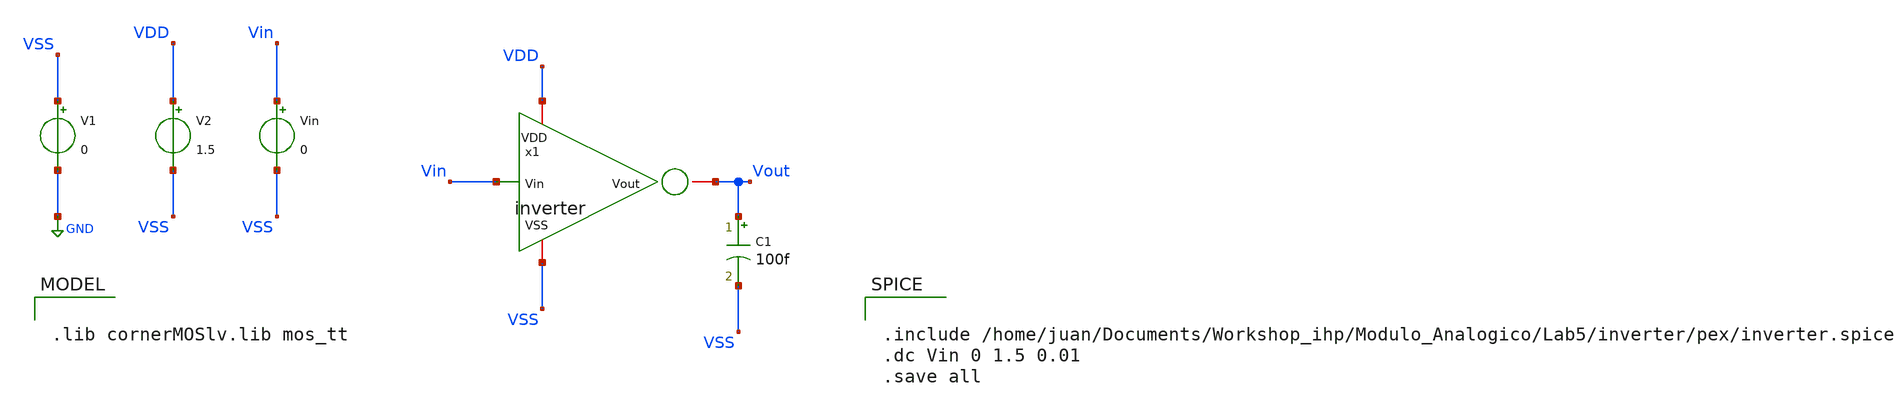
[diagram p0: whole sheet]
** sch_path: Modulo_Analogico/Lab5/inverter/pex/inverter_tb.sch
**.subckt inverter_tb
C1 Vout VSS 100f m=1
V1 VSS GND 0
V2 VDD VSS 1.5
Vin Vin VSS 0
x1 Vin VDD VSS Vout inverter
**** begin user architecture code


.include /home/juan/Documents/Workshop_ihp/Modulo_Analogico/Lab5/inverter/pex/inverter.spice
.dc Vin 0 1.5 0.01
.save all



.lib cornerMOSlv.lib mos_tt

**** end user architecture code
**.ends
.GLOBAL GND
.end
